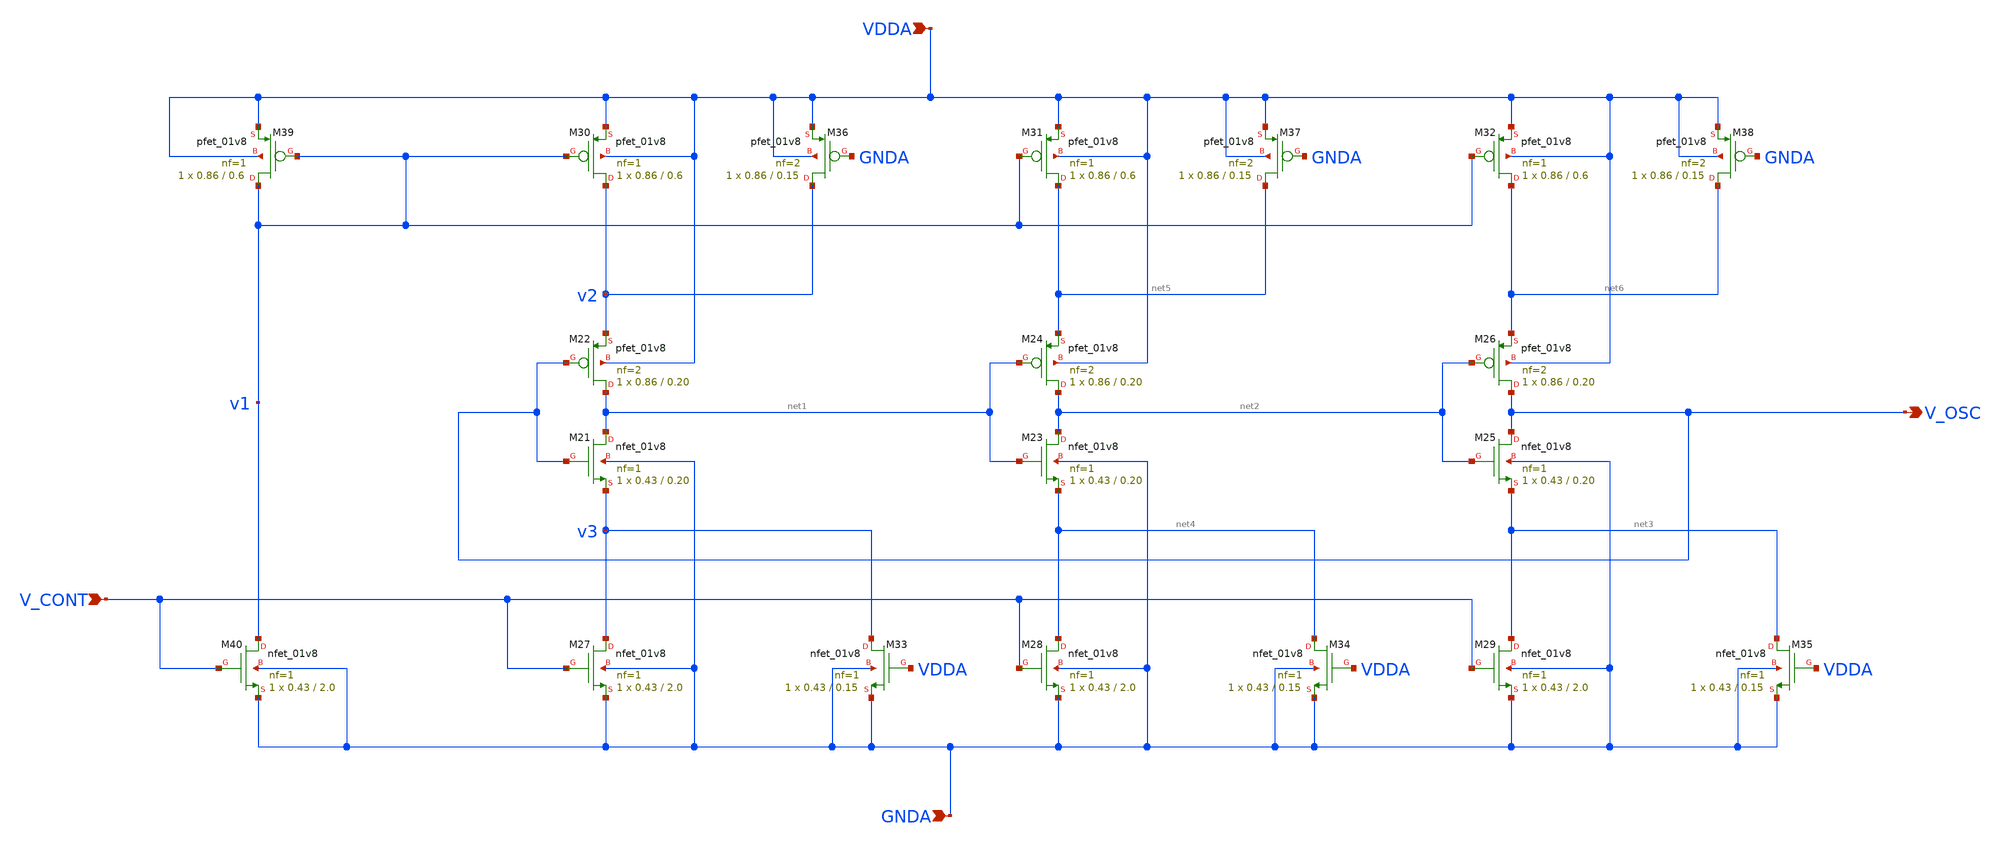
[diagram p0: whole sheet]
** sch_path: projects/pll/vco/xschem_ngspice/current_starved_VCO7.sch
**.subckt current_starved_VCO7 V_OSC VDDA GNDA V_CONT
*.opin V_OSC
*.ipin VDDA
*.ipin GNDA
*.ipin V_CONT
XM21 net1 V_OSC v3 GNDA sky130_fd_pr__nfet_01v8 L=0.20 W=0.43 nf=1 ad='int((nf+1)/2) * W/nf * 0.29' as='int((nf+2)/2) * W/nf * 0.29'
+ pd='2*int((nf+1)/2) * (W/nf + 0.29)' ps='2*int((nf+2)/2) * (W/nf + 0.29)' nrd='0.29 / W' nrs='0.29 / W'
+ sa=0 sb=0 sd=0 mult=1 m=1
XM22 net1 V_OSC v2 VDDA sky130_fd_pr__pfet_01v8 L=0.20 W=0.86 nf=2 ad='int((nf+1)/2) * W/nf * 0.29' as='int((nf+2)/2) * W/nf * 0.29'
+ pd='2*int((nf+1)/2) * (W/nf + 0.29)' ps='2*int((nf+2)/2) * (W/nf + 0.29)' nrd='0.29 / W' nrs='0.29 / W'
+ sa=0 sb=0 sd=0 mult=1 m=1
XM23 net2 net1 net4 GNDA sky130_fd_pr__nfet_01v8 L=0.20 W=0.43 nf=1 ad='int((nf+1)/2) * W/nf * 0.29'
+ as='int((nf+2)/2) * W/nf * 0.29' pd='2*int((nf+1)/2) * (W/nf + 0.29)' ps='2*int((nf+2)/2) * (W/nf + 0.29)'
+ nrd='0.29 / W' nrs='0.29 / W' sa=0 sb=0 sd=0 mult=1 m=1
XM24 net2 net1 net5 VDDA sky130_fd_pr__pfet_01v8 L=0.20 W=0.86 nf=2 ad='int((nf+1)/2) * W/nf * 0.29'
+ as='int((nf+2)/2) * W/nf * 0.29' pd='2*int((nf+1)/2) * (W/nf + 0.29)' ps='2*int((nf+2)/2) * (W/nf + 0.29)'
+ nrd='0.29 / W' nrs='0.29 / W' sa=0 sb=0 sd=0 mult=1 m=1
XM25 V_OSC net2 net3 GNDA sky130_fd_pr__nfet_01v8 L=0.20 W=0.43 nf=1 ad='int((nf+1)/2) * W/nf * 0.29'
+ as='int((nf+2)/2) * W/nf * 0.29' pd='2*int((nf+1)/2) * (W/nf + 0.29)' ps='2*int((nf+2)/2) * (W/nf + 0.29)'
+ nrd='0.29 / W' nrs='0.29 / W' sa=0 sb=0 sd=0 mult=1 m=1
XM26 V_OSC net2 net6 VDDA sky130_fd_pr__pfet_01v8 L=0.20 W=0.86 nf=2 ad='int((nf+1)/2) * W/nf * 0.29'
+ as='int((nf+2)/2) * W/nf * 0.29' pd='2*int((nf+1)/2) * (W/nf + 0.29)' ps='2*int((nf+2)/2) * (W/nf + 0.29)'
+ nrd='0.29 / W' nrs='0.29 / W' sa=0 sb=0 sd=0 mult=1 m=1
XM27 v3 V_CONT GNDA GNDA sky130_fd_pr__nfet_01v8 L=2.0 W=0.43 nf=1 ad='int((nf+1)/2) * W/nf * 0.29' as='int((nf+2)/2) * W/nf * 0.29'
+ pd='2*int((nf+1)/2) * (W/nf + 0.29)' ps='2*int((nf+2)/2) * (W/nf + 0.29)' nrd='0.29 / W' nrs='0.29 / W'
+ sa=0 sb=0 sd=0 mult=1 m=1
XM28 net4 V_CONT GNDA GNDA sky130_fd_pr__nfet_01v8 L=2.0 W=0.43 nf=1 ad='int((nf+1)/2) * W/nf * 0.29'
+ as='int((nf+2)/2) * W/nf * 0.29' pd='2*int((nf+1)/2) * (W/nf + 0.29)' ps='2*int((nf+2)/2) * (W/nf + 0.29)'
+ nrd='0.29 / W' nrs='0.29 / W' sa=0 sb=0 sd=0 mult=1 m=1
XM29 net3 V_CONT GNDA GNDA sky130_fd_pr__nfet_01v8 L=2.0 W=0.43 nf=1 ad='int((nf+1)/2) * W/nf * 0.29'
+ as='int((nf+2)/2) * W/nf * 0.29' pd='2*int((nf+1)/2) * (W/nf + 0.29)' ps='2*int((nf+2)/2) * (W/nf + 0.29)'
+ nrd='0.29 / W' nrs='0.29 / W' sa=0 sb=0 sd=0 mult=1 m=1
XM30 v2 v1 VDDA VDDA sky130_fd_pr__pfet_01v8 L=0.6 W=0.86 nf=1 ad='int((nf+1)/2) * W/nf * 0.29' as='int((nf+2)/2) * W/nf * 0.29'
+ pd='2*int((nf+1)/2) * (W/nf + 0.29)' ps='2*int((nf+2)/2) * (W/nf + 0.29)' nrd='0.29 / W' nrs='0.29 / W'
+ sa=0 sb=0 sd=0 mult=1 m=1
XM31 net5 v1 VDDA VDDA sky130_fd_pr__pfet_01v8 L=0.6 W=0.86 nf=1 ad='int((nf+1)/2) * W/nf * 0.29' as='int((nf+2)/2) * W/nf * 0.29'
+ pd='2*int((nf+1)/2) * (W/nf + 0.29)' ps='2*int((nf+2)/2) * (W/nf + 0.29)' nrd='0.29 / W' nrs='0.29 / W'
+ sa=0 sb=0 sd=0 mult=1 m=1
XM32 net6 v1 VDDA VDDA sky130_fd_pr__pfet_01v8 L=0.6 W=0.86 nf=1 ad='int((nf+1)/2) * W/nf * 0.29' as='int((nf+2)/2) * W/nf * 0.29'
+ pd='2*int((nf+1)/2) * (W/nf + 0.29)' ps='2*int((nf+2)/2) * (W/nf + 0.29)' nrd='0.29 / W' nrs='0.29 / W'
+ sa=0 sb=0 sd=0 mult=1 m=1
XM33 v3 VDDA GNDA GNDA sky130_fd_pr__nfet_01v8 L=0.15 W=0.43 nf=1 ad='int((nf+1)/2) * W/nf * 0.29' as='int((nf+2)/2) * W/nf * 0.29'
+ pd='2*int((nf+1)/2) * (W/nf + 0.29)' ps='2*int((nf+2)/2) * (W/nf + 0.29)' nrd='0.29 / W' nrs='0.29 / W'
+ sa=0 sb=0 sd=0 mult=1 m=1
XM34 net4 VDDA GNDA GNDA sky130_fd_pr__nfet_01v8 L=0.15 W=0.43 nf=1 ad='int((nf+1)/2) * W/nf * 0.29'
+ as='int((nf+2)/2) * W/nf * 0.29' pd='2*int((nf+1)/2) * (W/nf + 0.29)' ps='2*int((nf+2)/2) * (W/nf + 0.29)'
+ nrd='0.29 / W' nrs='0.29 / W' sa=0 sb=0 sd=0 mult=1 m=1
XM35 net3 VDDA GNDA GNDA sky130_fd_pr__nfet_01v8 L=0.15 W=0.43 nf=1 ad='int((nf+1)/2) * W/nf * 0.29'
+ as='int((nf+2)/2) * W/nf * 0.29' pd='2*int((nf+1)/2) * (W/nf + 0.29)' ps='2*int((nf+2)/2) * (W/nf + 0.29)'
+ nrd='0.29 / W' nrs='0.29 / W' sa=0 sb=0 sd=0 mult=1 m=1
XM36 v2 GNDA VDDA VDDA sky130_fd_pr__pfet_01v8 L=0.15 W=0.86 nf=2 ad='int((nf+1)/2) * W/nf * 0.29' as='int((nf+2)/2) * W/nf * 0.29'
+ pd='2*int((nf+1)/2) * (W/nf + 0.29)' ps='2*int((nf+2)/2) * (W/nf + 0.29)' nrd='0.29 / W' nrs='0.29 / W'
+ sa=0 sb=0 sd=0 mult=1 m=1
XM37 net5 GNDA VDDA VDDA sky130_fd_pr__pfet_01v8 L=0.15 W=0.86 nf=2 ad='int((nf+1)/2) * W/nf * 0.29'
+ as='int((nf+2)/2) * W/nf * 0.29' pd='2*int((nf+1)/2) * (W/nf + 0.29)' ps='2*int((nf+2)/2) * (W/nf + 0.29)'
+ nrd='0.29 / W' nrs='0.29 / W' sa=0 sb=0 sd=0 mult=1 m=1
XM38 net6 GNDA VDDA VDDA sky130_fd_pr__pfet_01v8 L=0.15 W=0.86 nf=2 ad='int((nf+1)/2) * W/nf * 0.29'
+ as='int((nf+2)/2) * W/nf * 0.29' pd='2*int((nf+1)/2) * (W/nf + 0.29)' ps='2*int((nf+2)/2) * (W/nf + 0.29)'
+ nrd='0.29 / W' nrs='0.29 / W' sa=0 sb=0 sd=0 mult=1 m=1
XM39 v1 v1 VDDA VDDA sky130_fd_pr__pfet_01v8 L=0.6 W=0.86 nf=1 ad='int((nf+1)/2) * W/nf * 0.29' as='int((nf+2)/2) * W/nf * 0.29'
+ pd='2*int((nf+1)/2) * (W/nf + 0.29)' ps='2*int((nf+2)/2) * (W/nf + 0.29)' nrd='0.29 / W' nrs='0.29 / W'
+ sa=0 sb=0 sd=0 mult=1 m=1
XM40 v1 V_CONT GNDA GNDA sky130_fd_pr__nfet_01v8 L=2.0 W=0.43 nf=1 ad='int((nf+1)/2) * W/nf * 0.29' as='int((nf+2)/2) * W/nf * 0.29'
+ pd='2*int((nf+1)/2) * (W/nf + 0.29)' ps='2*int((nf+2)/2) * (W/nf + 0.29)' nrd='0.29 / W' nrs='0.29 / W'
+ sa=0 sb=0 sd=0 mult=1 m=1
**.ends
.end
